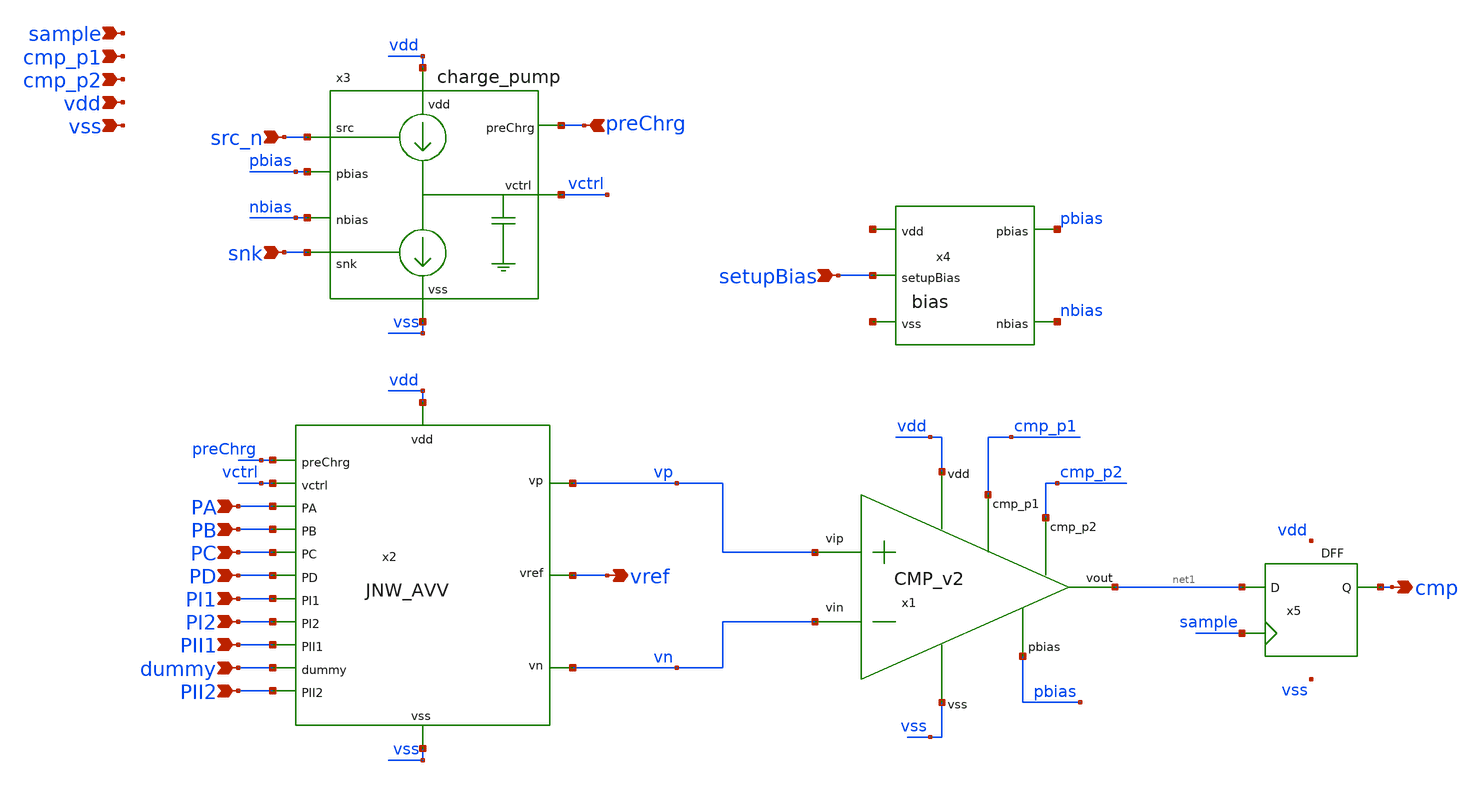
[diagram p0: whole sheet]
** sch_path: design/JNW_AVV_SKY130A/TB_bandgap.sch
**.subckt TB_bandgap vdd vss vref src_n snk PA PB PC PD PI1 PI2 PII1 cmp preChrg dummy PII2
*+ setupBias cmp_p1 cmp_p2 sample
*.ipin vdd
*.ipin vss
*.opin vref
*.ipin src_n
*.ipin snk
*.ipin PA
*.ipin PB
*.ipin PC
*.ipin PD
*.ipin PI1
*.ipin PI2
*.ipin PII1
*.opin cmp
*.ipin preChrg
*.ipin dummy
*.ipin PII2
*.ipin setupBias
*.ipin cmp_p1
*.ipin cmp_p2
*.ipin sample
x3 vdd pbias src_n vctrl snk nbias vss preChrg charge_pump
x2 vctrl PA PD vref vdd vss PC PB dummy PI2 PI1 PII1 vn vp PII2 preChrg JNW_AVV
x4 pbias net2 nbias net3 setupBias bias
x1 vdd pbias net1 vn vp vss cmp_p1 cmp_p2 CMP_v2
x5 cmp net1 sample VCC VSS VCC VSS DFF
**.ends
.end
